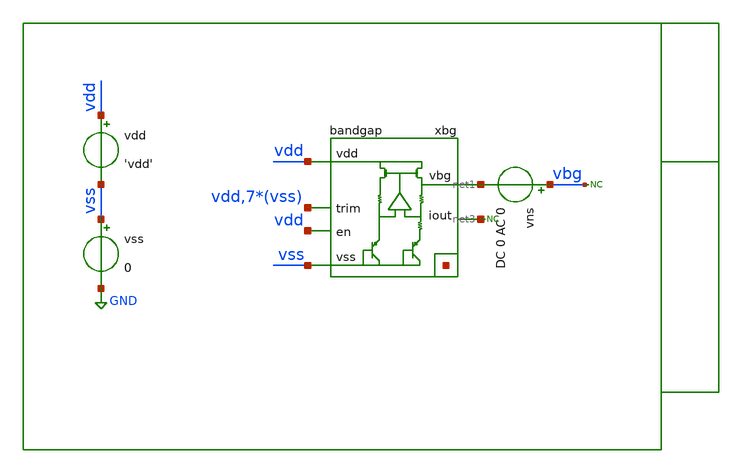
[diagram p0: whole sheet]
** sch_path: xschem/tb/bandgap_cm/bandgap/no_bandgap.sch
**.subckt no_bandgap
xbg vdd net1 vss net2[7] net2[6] net2[5] net2[4] net2[3] net2[2] net2[1] net2[0] vdd vss vss vss vss
+ vss vss vss net3 vdd bandgap
vdd vdd vss 'vdd'
vss vss GND 0
* noconn vbg
vns vbg net1 DC 0 AC 0
* noconn #net3
**** begin user architecture code

* Control

.param vdd = 5

.temp 27
.options reltol    = 1e-6

*------------------------------------------------------------
* Nodeset for better convergence
*------------------------------------------------------------
.nodeset v(vbg)  = '1'
.nodeset v(xbg.gate) = 'vdd/2'
.nodeset v(xbg.vx)   = '0.70'
.nodeset v(xbg.vbe2) = '0.65'
.nodeset v(xbg.vs1)  = '0'
*------------------------------------------------------------

.control

save all

noise v(vbg,vss) vns dec 10 0.1 10 1

print onoise_total
setplot noise1
gnuplot p1 onoise_spectrum
setplot noise1
set wr_vecnames
wrdata noise.csv all

.endc
.end


 * Model Corners

.include $::CORNERS/ngspice/tt.spice
*.include $::CORNERS/ngspice/ff.spice
*.include $::CORNERS/ngspice/ss.spice
*.include $::CORNERS/ngspice/sf.spice
*.include $::CORNERS/ngspice/fs.spice

**** end user architecture code
**.ends
.GLOBAL GND
.end
